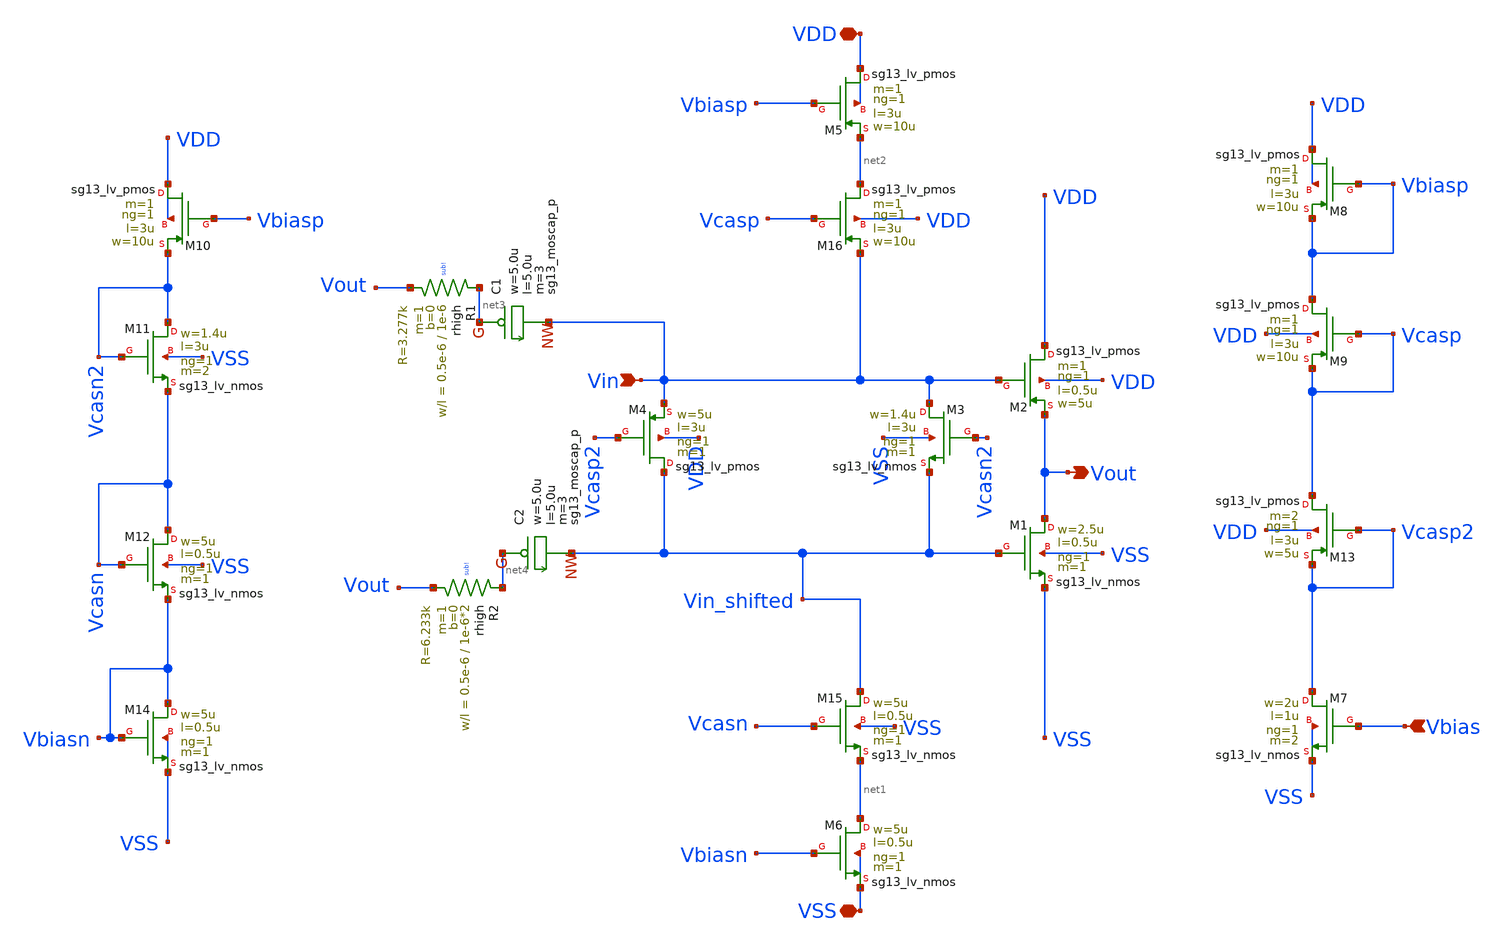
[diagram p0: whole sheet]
** sch_path: schema/ota_cmfb_core/ota_cmfb_core_push_pull_output_stage.sch
**.subckt ota_cmfb_core_push_pull_output_stage VSS VDD Vbias Vin Vout
*.iopin VSS
*.iopin VDD
*.ipin Vbias
*.ipin Vin
*.opin Vout
XM1 Vout Vin_shifted VSS VSS sg13_lv_nmos w=2.5u l=0.5u ng=1 m=1 mm_ok=1
XM2 VDD Vin Vout VDD sg13_lv_pmos w=5u l=0.5u ng=1 m=1 mm_ok=1
XM5 VDD Vbiasp net2 VDD sg13_lv_pmos w=10u l=3u ng=1 m=1 mm_ok=1
XM6 net1 Vbiasn VSS VSS sg13_lv_nmos w=5u l=0.5u ng=1 m=1 mm_ok=1
XM4 Vin_shifted Vcasp2 Vin VDD sg13_lv_pmos w=5u l=3u ng=1 m=1 mm_ok=1
XM15 Vin_shifted Vcasn net1 VSS sg13_lv_nmos w=5u l=0.5u ng=1 m=1 mm_ok=1
XM16 net2 Vcasp Vin VDD sg13_lv_pmos w=10u l=3u ng=1 m=1 mm_ok=1
XM3 Vin Vcasn2 Vin_shifted VSS sg13_lv_nmos w=1.4u l=3u ng=1 m=1 mm_ok=1
XM8 VDD Vbiasp Vbiasp VDD sg13_lv_pmos w=10u l=3u ng=1 m=1 mm_ok=1
XM9 Vbiasp Vcasp Vcasp VDD sg13_lv_pmos w=10u l=3u ng=1 m=1 mm_ok=1
XM13 Vcasp Vcasp2 Vcasp2 VDD sg13_lv_pmos w=5u l=3u ng=1 m=2 mm_ok=1
XM10 VDD Vbiasp Vcasn2 VDD sg13_lv_pmos w=10u l=3u ng=1 m=1 mm_ok=1
XM11 Vcasn2 Vcasn2 Vcasn VSS sg13_lv_nmos w=1.4u l=3u ng=1 m=2 mm_ok=1
XM12 Vcasn Vcasn Vbiasn VSS sg13_lv_nmos w=5u l=0.5u ng=1 m=1 mm_ok=1
XM14 Vbiasn Vbiasn VSS VSS sg13_lv_nmos w=5u l=0.5u ng=1 m=1 mm_ok=1
XM7 Vcasp2 Vbias VSS VSS sg13_lv_nmos w=2u l=1u ng=1 m=2 mm_ok=1
XR1 net3 Vout sub! rhigh w=0.5e-6 l=1e-6 m=1 b=0 mm_ok=1
XR2 net4 Vout sub! rhigh w=0.5e-6 l=1e-6*2 m=1 b=0 mm_ok=1
XC1 net3 Vin sg13_moscap_p w=5.0u l=5.0u m=3 mm_ok=1
XC2 net4 Vin_shifted sg13_moscap_p w=5.0u l=5.0u m=3 mm_ok=1
**.ends
.end
